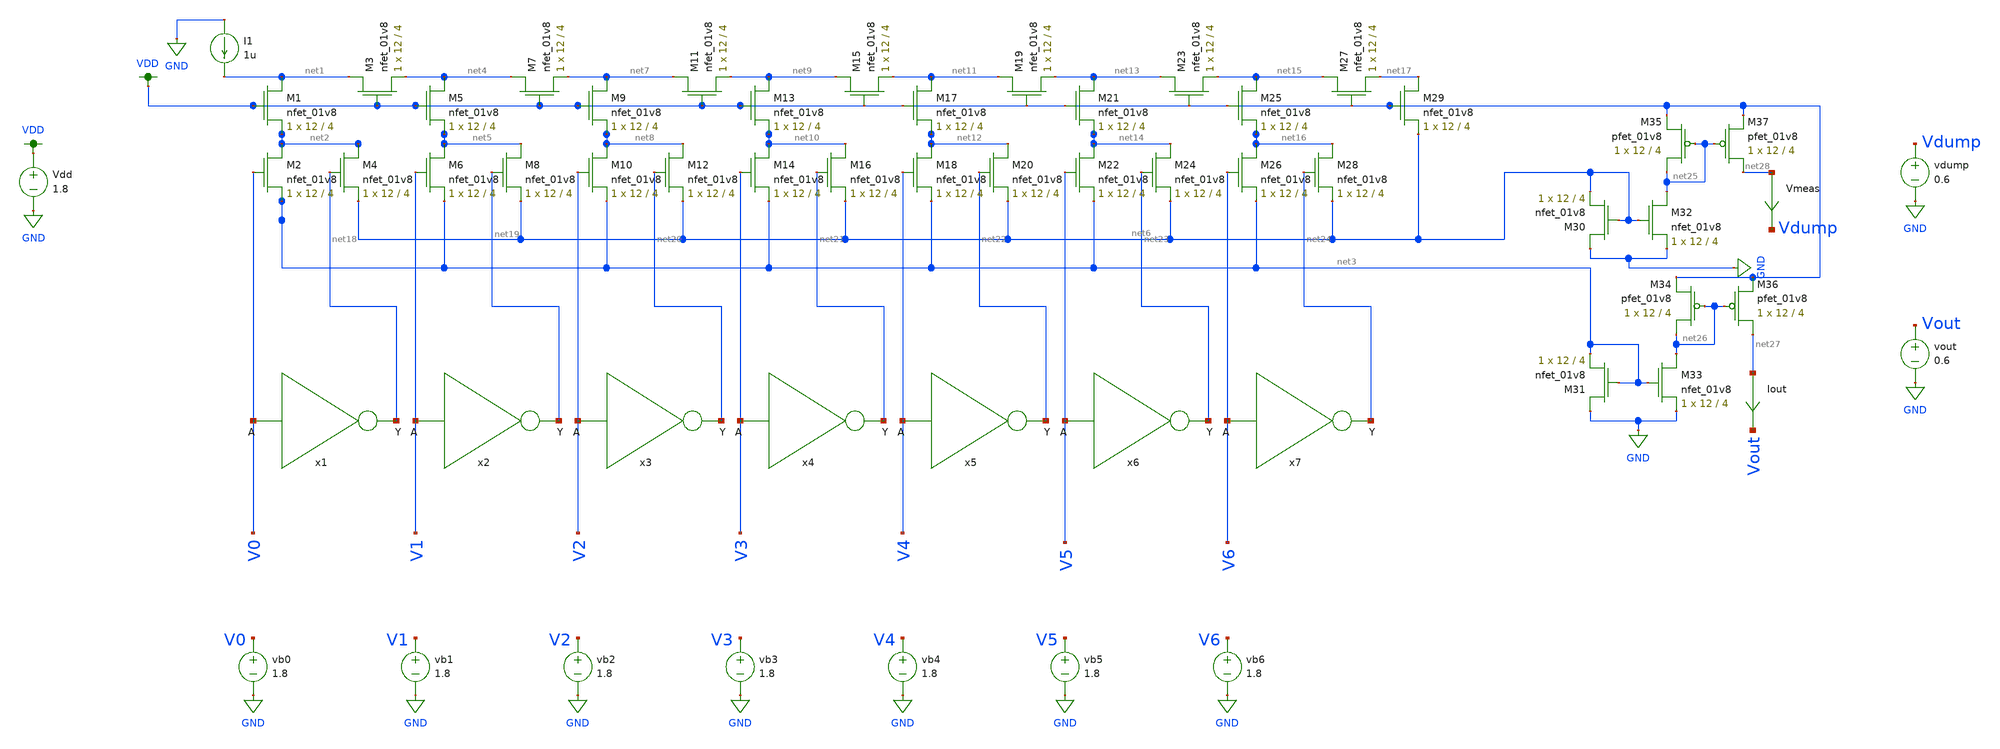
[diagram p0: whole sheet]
** sch_path: xschem/ladder_dac_simulation_andrew.sch
**.subckt ladder_dac_simulation_andrew
XM1 net1 VDD net2 GND sky130_fd_pr__nfet_01v8 L=4 W=12 nf=1 ad='int((nf+1)/2) * W/nf * 0.29' as='int((nf+2)/2) * W/nf * 0.29'
+ pd='2*int((nf+1)/2) * (W/nf + 0.29)' ps='2*int((nf+2)/2) * (W/nf + 0.29)' nrd='0.29 / W' nrs='0.29 / W'
+ sa=0 sb=0 sd=0 mult=1 m=1
XM3 net1 VDD net4 GND sky130_fd_pr__nfet_01v8 L=4 W=12 nf=1 ad='int((nf+1)/2) * W/nf * 0.29' as='int((nf+2)/2) * W/nf * 0.29'
+ pd='2*int((nf+1)/2) * (W/nf + 0.29)' ps='2*int((nf+2)/2) * (W/nf + 0.29)' nrd='0.29 / W' nrs='0.29 / W'
+ sa=0 sb=0 sd=0 mult=1 m=1
XM5 net4 VDD net5 GND sky130_fd_pr__nfet_01v8 L=4 W=12 nf=1 ad='int((nf+1)/2) * W/nf * 0.29' as='int((nf+2)/2) * W/nf * 0.29'
+ pd='2*int((nf+1)/2) * (W/nf + 0.29)' ps='2*int((nf+2)/2) * (W/nf + 0.29)' nrd='0.29 / W' nrs='0.29 / W'
+ sa=0 sb=0 sd=0 mult=1 m=1
XM7 net4 VDD net7 GND sky130_fd_pr__nfet_01v8 L=4 W=12 nf=1 ad='int((nf+1)/2) * W/nf * 0.29' as='int((nf+2)/2) * W/nf * 0.29'
+ pd='2*int((nf+1)/2) * (W/nf + 0.29)' ps='2*int((nf+2)/2) * (W/nf + 0.29)' nrd='0.29 / W' nrs='0.29 / W'
+ sa=0 sb=0 sd=0 mult=1 m=1
XM6 net5 V1 net3 GND sky130_fd_pr__nfet_01v8 L=4 W=12 nf=1 ad='int((nf+1)/2) * W/nf * 0.29' as='int((nf+2)/2) * W/nf * 0.29'
+ pd='2*int((nf+1)/2) * (W/nf + 0.29)' ps='2*int((nf+2)/2) * (W/nf + 0.29)' nrd='0.29 / W' nrs='0.29 / W'
+ sa=0 sb=0 sd=0 mult=1 m=1
XM8 net5 net19 net6 GND sky130_fd_pr__nfet_01v8 L=4 W=12 nf=1 ad='int((nf+1)/2) * W/nf * 0.29' as='int((nf+2)/2) * W/nf * 0.29'
+ pd='2*int((nf+1)/2) * (W/nf + 0.29)' ps='2*int((nf+2)/2) * (W/nf + 0.29)' nrd='0.29 / W' nrs='0.29 / W'
+ sa=0 sb=0 sd=0 mult=1 m=1
XM2 net2 V0 net3 GND sky130_fd_pr__nfet_01v8 L=4 W=12 nf=1 ad='int((nf+1)/2) * W/nf * 0.29' as='int((nf+2)/2) * W/nf * 0.29'
+ pd='2*int((nf+1)/2) * (W/nf + 0.29)' ps='2*int((nf+2)/2) * (W/nf + 0.29)' nrd='0.29 / W' nrs='0.29 / W'
+ sa=0 sb=0 sd=0 mult=1 m=1
XM4 net2 net18 net6 GND sky130_fd_pr__nfet_01v8 L=4 W=12 nf=1 ad='int((nf+1)/2) * W/nf * 0.29' as='int((nf+2)/2) * W/nf * 0.29'
+ pd='2*int((nf+1)/2) * (W/nf + 0.29)' ps='2*int((nf+2)/2) * (W/nf + 0.29)' nrd='0.29 / W' nrs='0.29 / W'
+ sa=0 sb=0 sd=0 mult=1 m=1
XM9 net7 VDD net8 GND sky130_fd_pr__nfet_01v8 L=4 W=12 nf=1 ad='int((nf+1)/2) * W/nf * 0.29' as='int((nf+2)/2) * W/nf * 0.29'
+ pd='2*int((nf+1)/2) * (W/nf + 0.29)' ps='2*int((nf+2)/2) * (W/nf + 0.29)' nrd='0.29 / W' nrs='0.29 / W'
+ sa=0 sb=0 sd=0 mult=1 m=1
XM11 net7 VDD net9 GND sky130_fd_pr__nfet_01v8 L=4 W=12 nf=1 ad='int((nf+1)/2) * W/nf * 0.29' as='int((nf+2)/2) * W/nf * 0.29'
+ pd='2*int((nf+1)/2) * (W/nf + 0.29)' ps='2*int((nf+2)/2) * (W/nf + 0.29)' nrd='0.29 / W' nrs='0.29 / W'
+ sa=0 sb=0 sd=0 mult=1 m=1
XM10 net8 V2 net3 GND sky130_fd_pr__nfet_01v8 L=4 W=12 nf=1 ad='int((nf+1)/2) * W/nf * 0.29' as='int((nf+2)/2) * W/nf * 0.29'
+ pd='2*int((nf+1)/2) * (W/nf + 0.29)' ps='2*int((nf+2)/2) * (W/nf + 0.29)' nrd='0.29 / W' nrs='0.29 / W'
+ sa=0 sb=0 sd=0 mult=1 m=1
XM12 net8 net20 net6 GND sky130_fd_pr__nfet_01v8 L=4 W=12 nf=1 ad='int((nf+1)/2) * W/nf * 0.29' as='int((nf+2)/2) * W/nf * 0.29'
+ pd='2*int((nf+1)/2) * (W/nf + 0.29)' ps='2*int((nf+2)/2) * (W/nf + 0.29)' nrd='0.29 / W' nrs='0.29 / W'
+ sa=0 sb=0 sd=0 mult=1 m=1
XM13 net9 VDD net10 GND sky130_fd_pr__nfet_01v8 L=4 W=12 nf=1 ad='int((nf+1)/2) * W/nf * 0.29' as='int((nf+2)/2) * W/nf * 0.29'
+ pd='2*int((nf+1)/2) * (W/nf + 0.29)' ps='2*int((nf+2)/2) * (W/nf + 0.29)' nrd='0.29 / W' nrs='0.29 / W'
+ sa=0 sb=0 sd=0 mult=1 m=1
XM15 net9 VDD net11 GND sky130_fd_pr__nfet_01v8 L=4 W=12 nf=1 ad='int((nf+1)/2) * W/nf * 0.29' as='int((nf+2)/2) * W/nf * 0.29'
+ pd='2*int((nf+1)/2) * (W/nf + 0.29)' ps='2*int((nf+2)/2) * (W/nf + 0.29)' nrd='0.29 / W' nrs='0.29 / W'
+ sa=0 sb=0 sd=0 mult=1 m=1
XM14 net10 V3 net3 GND sky130_fd_pr__nfet_01v8 L=4 W=12 nf=1 ad='int((nf+1)/2) * W/nf * 0.29' as='int((nf+2)/2) * W/nf * 0.29'
+ pd='2*int((nf+1)/2) * (W/nf + 0.29)' ps='2*int((nf+2)/2) * (W/nf + 0.29)' nrd='0.29 / W' nrs='0.29 / W'
+ sa=0 sb=0 sd=0 mult=1 m=1
XM16 net10 net21 net6 GND sky130_fd_pr__nfet_01v8 L=4 W=12 nf=1 ad='int((nf+1)/2) * W/nf * 0.29' as='int((nf+2)/2) * W/nf * 0.29'
+ pd='2*int((nf+1)/2) * (W/nf + 0.29)' ps='2*int((nf+2)/2) * (W/nf + 0.29)' nrd='0.29 / W' nrs='0.29 / W'
+ sa=0 sb=0 sd=0 mult=1 m=1
XM17 net11 VDD net12 GND sky130_fd_pr__nfet_01v8 L=4 W=12 nf=1 ad='int((nf+1)/2) * W/nf * 0.29' as='int((nf+2)/2) * W/nf * 0.29'
+ pd='2*int((nf+1)/2) * (W/nf + 0.29)' ps='2*int((nf+2)/2) * (W/nf + 0.29)' nrd='0.29 / W' nrs='0.29 / W'
+ sa=0 sb=0 sd=0 mult=1 m=1
XM19 net11 VDD net13 GND sky130_fd_pr__nfet_01v8 L=4 W=12 nf=1 ad='int((nf+1)/2) * W/nf * 0.29' as='int((nf+2)/2) * W/nf * 0.29'
+ pd='2*int((nf+1)/2) * (W/nf + 0.29)' ps='2*int((nf+2)/2) * (W/nf + 0.29)' nrd='0.29 / W' nrs='0.29 / W'
+ sa=0 sb=0 sd=0 mult=1 m=1
XM18 net12 V4 net3 GND sky130_fd_pr__nfet_01v8 L=4 W=12 nf=1 ad='int((nf+1)/2) * W/nf * 0.29' as='int((nf+2)/2) * W/nf * 0.29'
+ pd='2*int((nf+1)/2) * (W/nf + 0.29)' ps='2*int((nf+2)/2) * (W/nf + 0.29)' nrd='0.29 / W' nrs='0.29 / W'
+ sa=0 sb=0 sd=0 mult=1 m=1
XM20 net12 net22 net6 GND sky130_fd_pr__nfet_01v8 L=4 W=12 nf=1 ad='int((nf+1)/2) * W/nf * 0.29' as='int((nf+2)/2) * W/nf * 0.29'
+ pd='2*int((nf+1)/2) * (W/nf + 0.29)' ps='2*int((nf+2)/2) * (W/nf + 0.29)' nrd='0.29 / W' nrs='0.29 / W'
+ sa=0 sb=0 sd=0 mult=1 m=1
XM21 net13 VDD net14 GND sky130_fd_pr__nfet_01v8 L=4 W=12 nf=1 ad='int((nf+1)/2) * W/nf * 0.29' as='int((nf+2)/2) * W/nf * 0.29'
+ pd='2*int((nf+1)/2) * (W/nf + 0.29)' ps='2*int((nf+2)/2) * (W/nf + 0.29)' nrd='0.29 / W' nrs='0.29 / W'
+ sa=0 sb=0 sd=0 mult=1 m=1
XM23 net13 VDD net15 GND sky130_fd_pr__nfet_01v8 L=4 W=12 nf=1 ad='int((nf+1)/2) * W/nf * 0.29' as='int((nf+2)/2) * W/nf * 0.29'
+ pd='2*int((nf+1)/2) * (W/nf + 0.29)' ps='2*int((nf+2)/2) * (W/nf + 0.29)' nrd='0.29 / W' nrs='0.29 / W'
+ sa=0 sb=0 sd=0 mult=1 m=1
XM22 net14 V5 net3 GND sky130_fd_pr__nfet_01v8 L=4 W=12 nf=1 ad='int((nf+1)/2) * W/nf * 0.29' as='int((nf+2)/2) * W/nf * 0.29'
+ pd='2*int((nf+1)/2) * (W/nf + 0.29)' ps='2*int((nf+2)/2) * (W/nf + 0.29)' nrd='0.29 / W' nrs='0.29 / W'
+ sa=0 sb=0 sd=0 mult=1 m=1
XM24 net14 net23 net6 GND sky130_fd_pr__nfet_01v8 L=4 W=12 nf=1 ad='int((nf+1)/2) * W/nf * 0.29' as='int((nf+2)/2) * W/nf * 0.29'
+ pd='2*int((nf+1)/2) * (W/nf + 0.29)' ps='2*int((nf+2)/2) * (W/nf + 0.29)' nrd='0.29 / W' nrs='0.29 / W'
+ sa=0 sb=0 sd=0 mult=1 m=1
XM25 net15 VDD net16 GND sky130_fd_pr__nfet_01v8 L=4 W=12 nf=1 ad='int((nf+1)/2) * W/nf * 0.29' as='int((nf+2)/2) * W/nf * 0.29'
+ pd='2*int((nf+1)/2) * (W/nf + 0.29)' ps='2*int((nf+2)/2) * (W/nf + 0.29)' nrd='0.29 / W' nrs='0.29 / W'
+ sa=0 sb=0 sd=0 mult=1 m=1
XM27 net15 VDD net17 GND sky130_fd_pr__nfet_01v8 L=4 W=12 nf=1 ad='int((nf+1)/2) * W/nf * 0.29' as='int((nf+2)/2) * W/nf * 0.29'
+ pd='2*int((nf+1)/2) * (W/nf + 0.29)' ps='2*int((nf+2)/2) * (W/nf + 0.29)' nrd='0.29 / W' nrs='0.29 / W'
+ sa=0 sb=0 sd=0 mult=1 m=1
XM26 net16 V6 net3 GND sky130_fd_pr__nfet_01v8 L=4 W=12 nf=1 ad='int((nf+1)/2) * W/nf * 0.29' as='int((nf+2)/2) * W/nf * 0.29'
+ pd='2*int((nf+1)/2) * (W/nf + 0.29)' ps='2*int((nf+2)/2) * (W/nf + 0.29)' nrd='0.29 / W' nrs='0.29 / W'
+ sa=0 sb=0 sd=0 mult=1 m=1
XM28 net16 net24 net6 GND sky130_fd_pr__nfet_01v8 L=4 W=12 nf=1 ad='int((nf+1)/2) * W/nf * 0.29' as='int((nf+2)/2) * W/nf * 0.29'
+ pd='2*int((nf+1)/2) * (W/nf + 0.29)' ps='2*int((nf+2)/2) * (W/nf + 0.29)' nrd='0.29 / W' nrs='0.29 / W'
+ sa=0 sb=0 sd=0 mult=1 m=1
XM29 net17 VDD net6 GND sky130_fd_pr__nfet_01v8 L=4 W=12 nf=1 ad='int((nf+1)/2) * W/nf * 0.29' as='int((nf+2)/2) * W/nf * 0.29'
+ pd='2*int((nf+1)/2) * (W/nf + 0.29)' ps='2*int((nf+2)/2) * (W/nf + 0.29)' nrd='0.29 / W' nrs='0.29 / W'
+ sa=0 sb=0 sd=0 mult=1 m=1
x1 net18 V0 inverter
x2 net19 V1 inverter
x3 net20 V2 inverter
x4 net21 V3 inverter
x5 net22 V4 inverter
x6 net23 V5 inverter
x7 net24 V6 inverter
XM30 GND net6 net6 GND sky130_fd_pr__nfet_01v8 L=4 W=12 nf=1 ad='int((nf+1)/2) * W/nf * 0.29' as='int((nf+2)/2) * W/nf * 0.29'
+ pd='2*int((nf+1)/2) * (W/nf + 0.29)' ps='2*int((nf+2)/2) * (W/nf + 0.29)' nrd='0.29 / W' nrs='0.29 / W'
+ sa=0 sb=0 sd=0 mult=1 m=1
XM31 GND net3 net3 GND sky130_fd_pr__nfet_01v8 L=4 W=12 nf=1 ad='int((nf+1)/2) * W/nf * 0.29' as='int((nf+2)/2) * W/nf * 0.29'
+ pd='2*int((nf+1)/2) * (W/nf + 0.29)' ps='2*int((nf+2)/2) * (W/nf + 0.29)' nrd='0.29 / W' nrs='0.29 / W'
+ sa=0 sb=0 sd=0 mult=1 m=1
XM32 net25 net6 GND GND sky130_fd_pr__nfet_01v8 L=4 W=12 nf=1 ad='int((nf+1)/2) * W/nf * 0.29' as='int((nf+2)/2) * W/nf * 0.29'
+ pd='2*int((nf+1)/2) * (W/nf + 0.29)' ps='2*int((nf+2)/2) * (W/nf + 0.29)' nrd='0.29 / W' nrs='0.29 / W'
+ sa=0 sb=0 sd=0 mult=1 m=1
XM33 net26 net3 GND GND sky130_fd_pr__nfet_01v8 L=4 W=12 nf=1 ad='int((nf+1)/2) * W/nf * 0.29' as='int((nf+2)/2) * W/nf * 0.29'
+ pd='2*int((nf+1)/2) * (W/nf + 0.29)' ps='2*int((nf+2)/2) * (W/nf + 0.29)' nrd='0.29 / W' nrs='0.29 / W'
+ sa=0 sb=0 sd=0 mult=1 m=1
XM35 net25 net25 VDD VDD sky130_fd_pr__pfet_01v8 L=4 W=12 nf=1 ad='int((nf+1)/2) * W/nf * 0.29' as='int((nf+2)/2) * W/nf * 0.29'
+ pd='2*int((nf+1)/2) * (W/nf + 0.29)' ps='2*int((nf+2)/2) * (W/nf + 0.29)' nrd='0.29 / W' nrs='0.29 / W'
+ sa=0 sb=0 sd=0 mult=1 m=1
XM37 net28 net25 VDD VDD sky130_fd_pr__pfet_01v8 L=4 W=12 nf=1 ad='int((nf+1)/2) * W/nf * 0.29' as='int((nf+2)/2) * W/nf * 0.29'
+ pd='2*int((nf+1)/2) * (W/nf + 0.29)' ps='2*int((nf+2)/2) * (W/nf + 0.29)' nrd='0.29 / W' nrs='0.29 / W'
+ sa=0 sb=0 sd=0 mult=1 m=1
XM34 net26 net26 VDD VDD sky130_fd_pr__pfet_01v8 L=4 W=12 nf=1 ad='int((nf+1)/2) * W/nf * 0.29' as='int((nf+2)/2) * W/nf * 0.29'
+ pd='2*int((nf+1)/2) * (W/nf + 0.29)' ps='2*int((nf+2)/2) * (W/nf + 0.29)' nrd='0.29 / W' nrs='0.29 / W'
+ sa=0 sb=0 sd=0 mult=1 m=1
XM36 net27 net26 VDD VDD sky130_fd_pr__pfet_01v8 L=4 W=12 nf=1 ad='int((nf+1)/2) * W/nf * 0.29' as='int((nf+2)/2) * W/nf * 0.29'
+ pd='2*int((nf+1)/2) * (W/nf + 0.29)' ps='2*int((nf+2)/2) * (W/nf + 0.29)' nrd='0.29 / W' nrs='0.29 / W'
+ sa=0 sb=0 sd=0 mult=1 m=1
I1 GND net1 1u
Vdd VDD GND 1.8
vb0 V0 GND 1.8
vb1 V1 GND 1.8
vb2 V2 GND 1.8
vb3 V3 GND 1.8
vb4 V4 GND 1.8
vb5 V5 GND 1.8
vb6 V6 GND 1.8
vdump Vdump GND 0.6
vout Vout GND 0.6
Vmeas net28 Vdump 0
.save i(vmeas)
Iout net27 Vout 0
.save i(iout)
**** begin user architecture code

.option wnflag=1
.param MC_SWITCH=0.0
.lib ~/skywater/skywater-pdk/libraries/sky130_fd_pr_ngspice/latest/models/sky130.lib.spice tt



.control
  set wr_vecnames
  set wr_singlescale
  let code = 0
  while code < 128
    if code eq 0
      let b0 = 0
    else
      let b0 = code % 2
    end
    if floor(code / 2) eq 0
      let b1 = 0
    else
      let b1 = floor(code / 2) % 2
    end
    if floor(code / 4) eq 0
      let b2 = 0
    else
      let b2 = floor(code / 4) % 2
    end
    if floor(code / 8) eq 0
      let b3 = 0
    else
      let b3 = floor(code / 8) % 2
    end
    if floor(code / 16) eq 0
      let b4 = 0
    else
      let b4 = floor(code / 16) % 2
    end
    if floor(code / 32) eq 0
      let b5 = 0
    else
      let b5 = floor(code / 32) % 2
    end
    if floor(code / 64) eq 0
      let b6 = 0
    else
      let b6 = floor(code / 64) % 2
    end
    alter Vb0 1.8*$&b0
    alter Vb1 1.8*$&b1
    alter Vb2 1.8*$&b2
    alter Vb3 1.8*$&b3
    alter Vb4 1.8*$&b4
    alter Vb5 1.8*$&b5
    alter Vb6 1.8*$&b6
    save all
    op
    wrdata ~/Documents/DAC-VLSI/simulation_results/ladder_dac_simulation_andrew.txt v(b0) v(b1)
+ v(b2) v(b3) v(b4) v(b5) v(b6) i(Iout)
    if code eq 0
      set appendwrite
      set wr_vecnames = FALSE
    end
    let code = code + 1
  end
  quit
.endc

**** end user architecture code
**.ends

* expanding   symbol:  ./inverter.sym # of pins=2
** sym_path: xschem/inverter.sym
** sch_path: xschem/inverter.sch
.subckt inverter Y A
*.ipin A
*.opin Y
XM1 Y A VDD VDD sky130_fd_pr__pfet_01v8 L=0.15 W=1 nf=1 ad='int((nf+1)/2) * W/nf * 0.29' as='int((nf+2)/2) * W/nf * 0.29'
+ pd='2*int((nf+1)/2) * (W/nf + 0.29)' ps='2*int((nf+2)/2) * (W/nf + 0.29)' nrd='0.29 / W' nrs='0.29 / W'
+ sa=0 sb=0 sd=0 mult=1 m=1
XM2 Y A GND GND sky130_fd_pr__nfet_01v8 L=0.15 W=1 nf=1 ad='int((nf+1)/2) * W/nf * 0.29' as='int((nf+2)/2) * W/nf * 0.29'
+ pd='2*int((nf+1)/2) * (W/nf + 0.29)' ps='2*int((nf+2)/2) * (W/nf + 0.29)' nrd='0.29 / W' nrs='0.29 / W'
+ sa=0 sb=0 sd=0 mult=1 m=1
.ends

.GLOBAL VDD
.GLOBAL GND
.end
